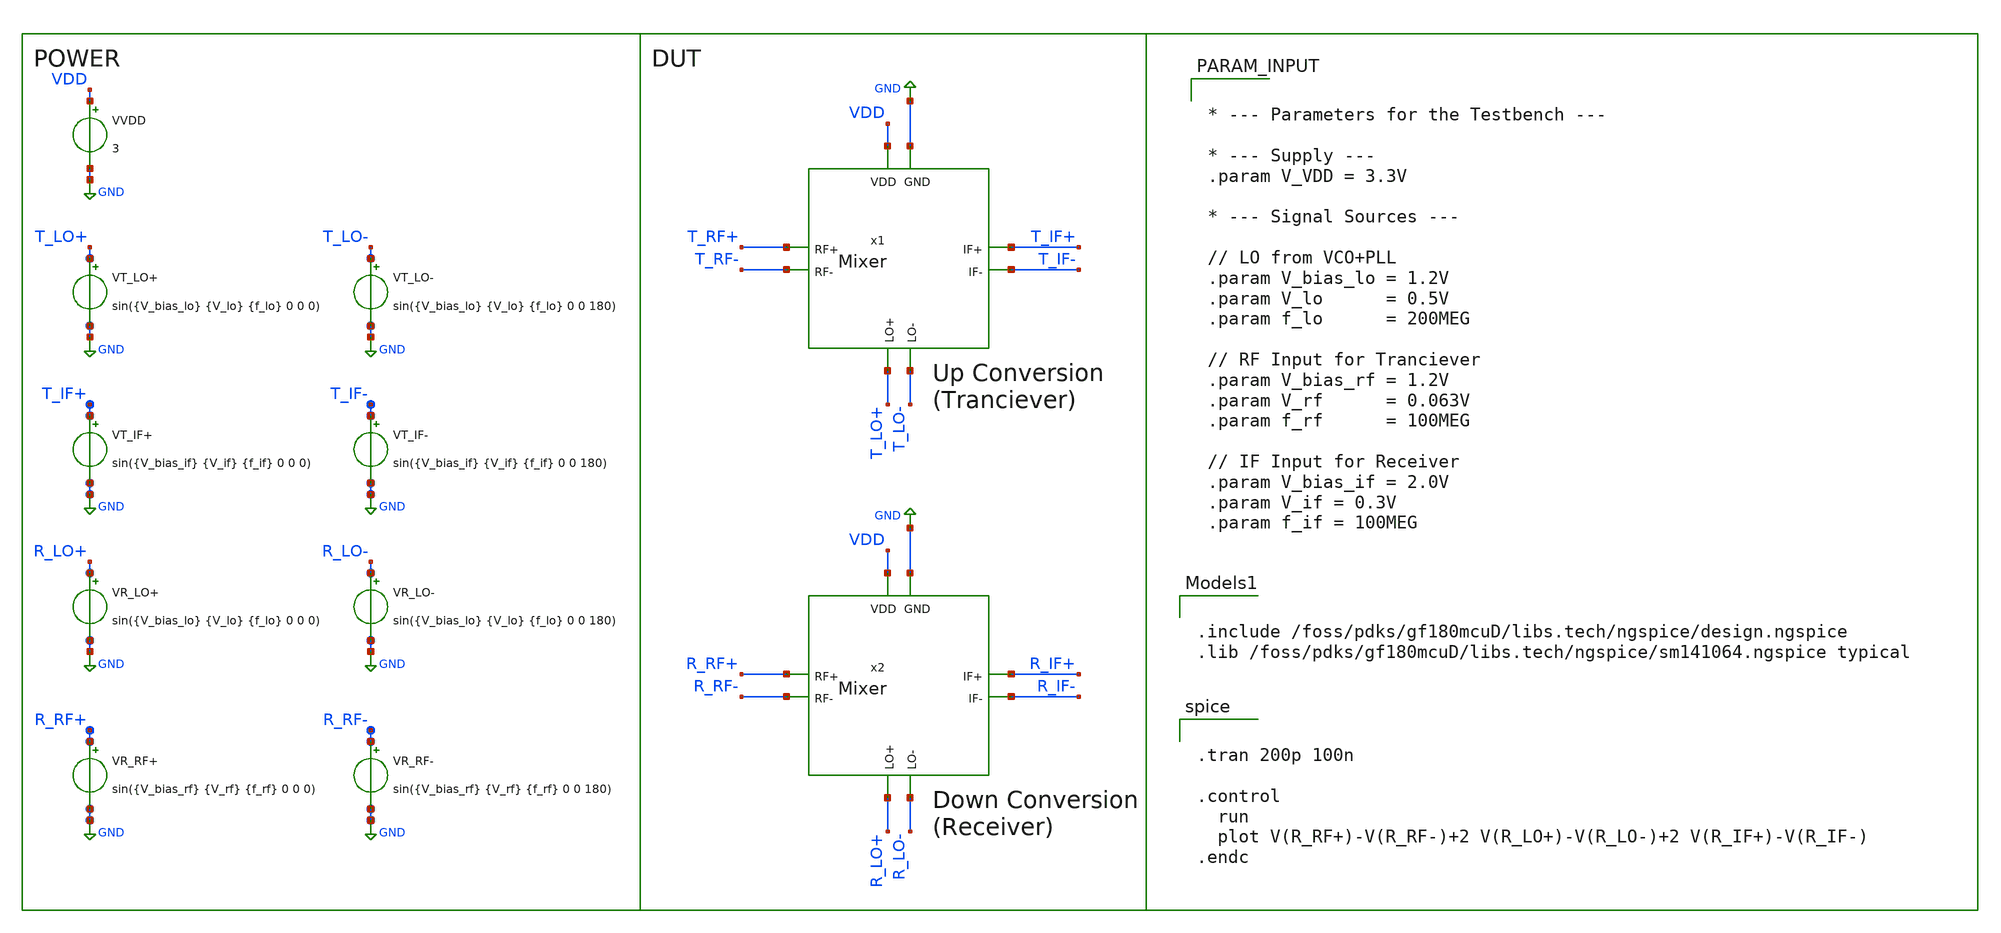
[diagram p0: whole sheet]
** sch_path: Project/1-on-chip/schematic/Mixer/tb_Mixer.sch
**.subckt tb_Mixer
VVDD VDD GND 3
VT_LO+ T_LO+ GND sin({V_bias_lo} {V_lo} {f_lo} 0 0 0)
VT_LO- T_LO- GND sin({V_bias_lo} {V_lo} {f_lo} 0 0 180)
VT_IF+ T_IF+ GND sin({V_bias_if} {V_if} {f_if} 0 0 0)
VT_IF- T_IF- GND sin({V_bias_if} {V_if} {f_if} 0 0 180)
VR_LO+ R_LO+ GND sin({V_bias_lo} {V_lo} {f_lo} 0 0 0)
VR_LO- R_LO- GND sin({V_bias_lo} {V_lo} {f_lo} 0 0 180)
VR_RF+ R_RF+ GND sin({V_bias_rf} {V_rf} {f_rf} 0 0 0)
VR_RF- R_RF- GND sin({V_bias_rf} {V_rf} {f_rf} 0 0 180)
x1 VDD GND T_LO+ T_LO- T_RF+ T_RF- T_IF+ T_IF- Mixer
x2 VDD GND R_LO+ R_LO- R_RF+ R_RF- R_IF+ R_IF- Mixer
**** begin user architecture code


.tran 200p 100n

.control
  run
  plot V(R_RF+)-V(R_RF-)+2 V(R_LO+)-V(R_LO-)+2 V(R_IF+)-V(R_IF-)
.endc



.include /foss/pdks/gf180mcuD/libs.tech/ngspice/design.ngspice
.lib /foss/pdks/gf180mcuD/libs.tech/ngspice/sm141064.ngspice typical



* --- Parameters for the Testbench ---

* --- Supply ---
.param V_VDD = 3.3V

* --- Signal Sources ---

// LO from VCO+PLL
.param V_bias_lo = 1.2V
.param V_lo      = 0.5V
.param f_lo      = 200MEG

// RF Input for Tranciever
.param V_bias_rf = 1.2V
.param V_rf      = 0.063V
.param f_rf      = 100MEG

// IF Input for Receiver
.param V_bias_if = 2.0V
.param V_if = 0.3V
.param f_if = 100MEG



**** end user architecture code
**.ends

* expanding   symbol:  Mixer.sym # of pins=8
** sym_path: Project/1-on-chip/schematic/Mixer/Mixer.sym
** sch_path: Project/1-on-chip/schematic/Mixer/Mixer.sch
.subckt Mixer VDD GND LO+ LO- RF+ RF- IF+ IF-
*.ipin GND
*.ipin VDD
*.ipin LO+
*.ipin LO-
*.iopin RF+
*.iopin RF-
*.iopin IF+
*.iopin IF-
XM8 net1 net1 GND GND nfet_03v3 L={L_min} W={W_bias_ref} nf=1 ad='int((nf+1)/2) * W/nf * 0.18u' as='int((nf+2)/2) * W/nf * 0.18u'
+ pd='2*int((nf+1)/2) * (W/nf + 0.18u)' ps='2*int((nf+2)/2) * (W/nf + 0.18u)' nrd='0.18u / W' nrs='0.18u / W'
+ sa=0 sb=0 sd=0 m=1
XM1 net2 net1 GND GND nfet_03v3 L={L_min} W={W_bias_out} nf=1 ad='int((nf+1)/2) * W/nf * 0.18u' as='int((nf+2)/2) * W/nf * 0.18u'
+ pd='2*int((nf+1)/2) * (W/nf + 0.18u)' ps='2*int((nf+2)/2) * (W/nf + 0.18u)' nrd='0.18u / W' nrs='0.18u / W'
+ sa=0 sb=0 sd=0 m=1
XM3 net8 net4 net2 GND nfet_03v3 L={L_min} W={W_rf} nf=1 ad='int((nf+1)/2) * W/nf * 0.18u' as='int((nf+2)/2) * W/nf * 0.18u'
+ pd='2*int((nf+1)/2) * (W/nf + 0.18u)' ps='2*int((nf+2)/2) * (W/nf + 0.18u)' nrd='0.18u / W' nrs='0.18u / W'
+ sa=0 sb=0 sd=0 m=1
XM2 net7 net6 net2 GND nfet_03v3 L={L_min} W={W_rf} nf=1 ad='int((nf+1)/2) * W/nf * 0.18u' as='int((nf+2)/2) * W/nf * 0.18u'
+ pd='2*int((nf+1)/2) * (W/nf + 0.18u)' ps='2*int((nf+2)/2) * (W/nf + 0.18u)' nrd='0.18u / W' nrs='0.18u / W'
+ sa=0 sb=0 sd=0 m=1
CGS2 net4 net2 {C_gate} m=1
LG2 net3 RF- {L_gate} m=1
CGS1 net6 net2 {C_gate} m=1
LG1 RF+ net5 {L_gate} m=1
RG1 net5 net6 {R_gate} m=1
RG2 net4 net3 {R_gate} m=1
XM7 IF- LO+ net8 GND nfet_03v3 L={L_min} W={W_sw} nf=1 ad='int((nf+1)/2) * W/nf * 0.18u' as='int((nf+2)/2) * W/nf * 0.18u'
+ pd='2*int((nf+1)/2) * (W/nf + 0.18u)' ps='2*int((nf+2)/2) * (W/nf + 0.18u)' nrd='0.18u / W' nrs='0.18u / W'
+ sa=0 sb=0 sd=0 m=1
XM6 IF+ LO- net8 GND nfet_03v3 L={L_min} W={W_sw} nf=1 ad='int((nf+1)/2) * W/nf * 0.18u' as='int((nf+2)/2) * W/nf * 0.18u'
+ pd='2*int((nf+1)/2) * (W/nf + 0.18u)' ps='2*int((nf+2)/2) * (W/nf + 0.18u)' nrd='0.18u / W' nrs='0.18u / W'
+ sa=0 sb=0 sd=0 m=1
XM5 IF- LO- net7 GND nfet_03v3 L={L_min} W={W_sw} nf=1 ad='int((nf+1)/2) * W/nf * 0.18u' as='int((nf+2)/2) * W/nf * 0.18u'
+ pd='2*int((nf+1)/2) * (W/nf + 0.18u)' ps='2*int((nf+2)/2) * (W/nf + 0.18u)' nrd='0.18u / W' nrs='0.18u / W'
+ sa=0 sb=0 sd=0 m=1
XM4 IF+ LO+ net7 GND nfet_03v3 L={L_min} W={W_sw} nf=1 ad='int((nf+1)/2) * W/nf * 0.18u' as='int((nf+2)/2) * W/nf * 0.18u'
+ pd='2*int((nf+1)/2) * (W/nf + 0.18u)' ps='2*int((nf+2)/2) * (W/nf + 0.18u)' nrd='0.18u / W' nrs='0.18u / W'
+ sa=0 sb=0 sd=0 m=1
RD2 VDD IF- {R_load} m=1
RD1 VDD IF+ {R_load} m=1
Rbias VDD net1 {R_bias} m=1
**** begin user architecture code


* --- Transistor Length ---
.param L_min = 0.28u

* --- Transistor W/L Ratios ---
.param WL_rf_ratio       = 80
.param WL_sw_ratio       = 40
.param WL_bias_ref_ratio = 10
.param WL_bias_out_ratio = 60

* --- Resistors ---
.param R_load = 600
.param R_bias = 7.5k

* --- Impedance Matching ---
.param R_gate = 50
.param C_gate = 4.7p
.param L_gate = 950n

* --- Calculated Transistor Widths ---
.param W_rf       = {WL_rf_ratio * L_min}
.param W_sw       = {WL_sw_ratio * L_min}
.param W_bias_ref = {WL_bias_ref_ratio * L_min}
.param W_bias_out = {WL_bias_out_ratio * L_min}




**** end user architecture code
I0 net9 net10 2m
.ends

.GLOBAL GND
.end
